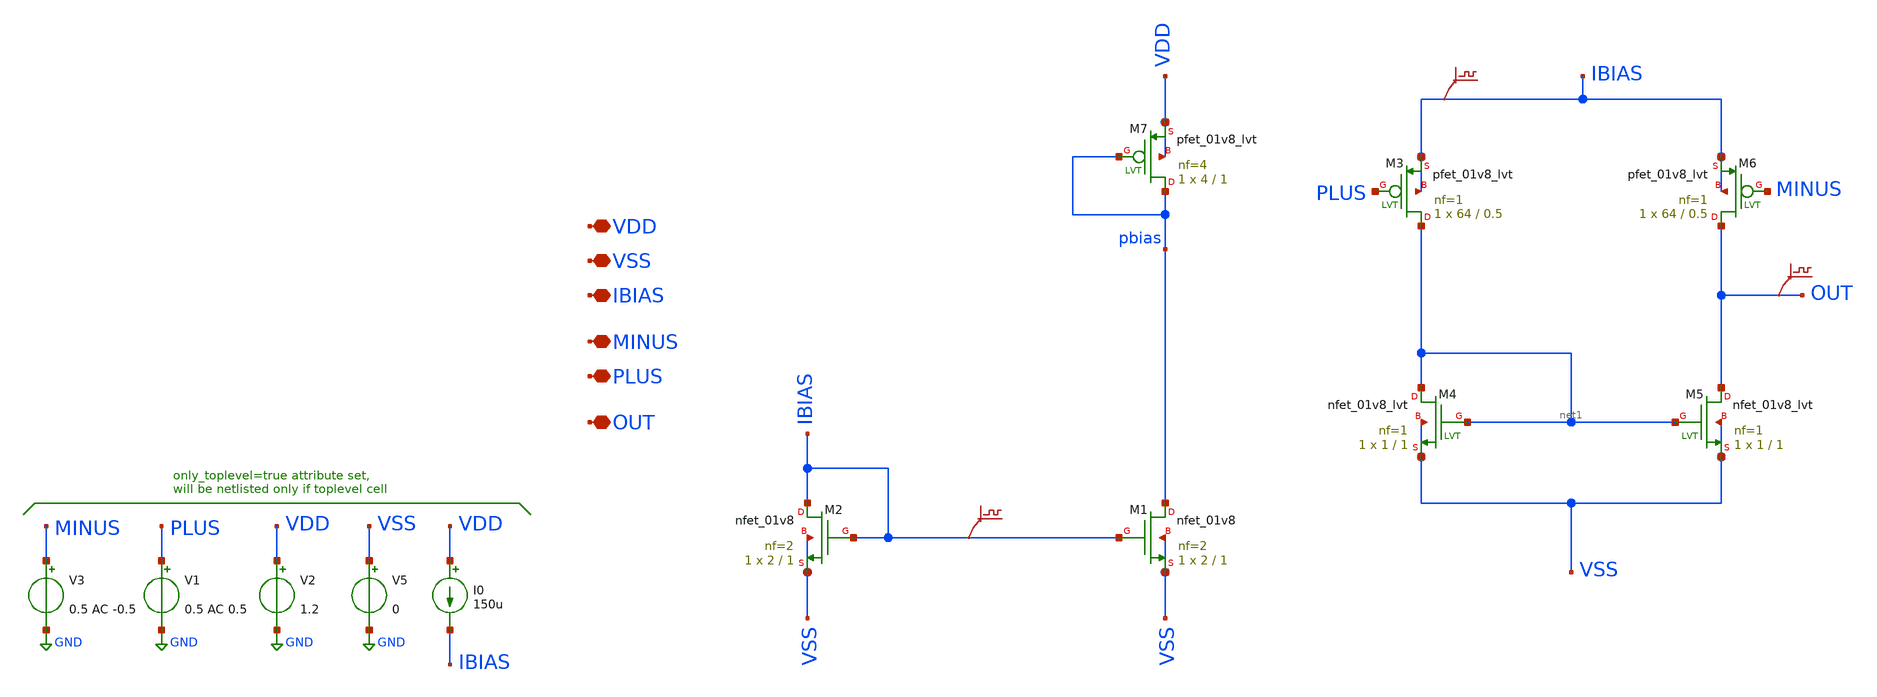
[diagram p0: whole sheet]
** sch_path: q2_opamp.sch
**.subckt q2_opamp VDD VSS MINUS PLUS OUT IBIAS
*.iopin VDD
*.iopin VSS
*.iopin MINUS
*.iopin PLUS
*.iopin OUT
*.iopin IBIAS
V1 PLUS GND 0.5 AC 0.5
V3 MINUS GND 0.5 AC -0.5
V5 VSS GND 0
I0 VDD IBIAS 150u
XM2 IBIAS IBIAS VSS VSS sky130_fd_pr__nfet_01v8 L=1 W=2 nf=2 ad='int((nf+1)/2) * W/nf * 0.29' as='int((nf+2)/2) * W/nf * 0.29'
+ pd='2*int((nf+1)/2) * (W/nf + 0.29)' ps='2*int((nf+2)/2) * (W/nf + 0.29)' nrd='0.29 / W' nrs='0.29 / W'
+ sa=0 sb=0 sd=0 mult=1 m=1
XM1 pbias IBIAS VSS VSS sky130_fd_pr__nfet_01v8 L=1 W=2 nf=2 ad='int((nf+1)/2) * W/nf * 0.29' as='int((nf+2)/2) * W/nf * 0.29'
+ pd='2*int((nf+1)/2) * (W/nf + 0.29)' ps='2*int((nf+2)/2) * (W/nf + 0.29)' nrd='0.29 / W' nrs='0.29 / W'
+ sa=0 sb=0 sd=0 mult=1 m=1
.save v(ibias)
V2 VDD GND 1.2
.save v(out)
XM4 net1 net1 VSS VSS sky130_fd_pr__nfet_01v8_lvt L=1 W=1 nf=1 ad='int((nf+1)/2) * W/nf * 0.29' as='int((nf+2)/2) * W/nf * 0.29'
+ pd='2*int((nf+1)/2) * (W/nf + 0.29)' ps='2*int((nf+2)/2) * (W/nf + 0.29)' nrd='0.29 / W' nrs='0.29 / W'
+ sa=0 sb=0 sd=0 mult=1 m=1
XM5 OUT net1 VSS VSS sky130_fd_pr__nfet_01v8_lvt L=1 W=1 nf=1 ad='int((nf+1)/2) * W/nf * 0.29' as='int((nf+2)/2) * W/nf * 0.29'
+ pd='2*int((nf+1)/2) * (W/nf + 0.29)' ps='2*int((nf+2)/2) * (W/nf + 0.29)' nrd='0.29 / W' nrs='0.29 / W'
+ sa=0 sb=0 sd=0 mult=1 m=1
XM3 net1 PLUS IBIAS IBIAS sky130_fd_pr__pfet_01v8_lvt L=0.5 W=64 nf=1 ad='int((nf+1)/2) * W/nf * 0.29'
+ as='int((nf+2)/2) * W/nf * 0.29' pd='2*int((nf+1)/2) * (W/nf + 0.29)' ps='2*int((nf+2)/2) * (W/nf + 0.29)'
+ nrd='0.29 / W' nrs='0.29 / W' sa=0 sb=0 sd=0 mult=1 m=1
XM6 OUT MINUS IBIAS IBIAS sky130_fd_pr__pfet_01v8_lvt L=0.5 W=64 nf=1 ad='int((nf+1)/2) * W/nf * 0.29'
+ as='int((nf+2)/2) * W/nf * 0.29' pd='2*int((nf+1)/2) * (W/nf + 0.29)' ps='2*int((nf+2)/2) * (W/nf + 0.29)'
+ nrd='0.29 / W' nrs='0.29 / W' sa=0 sb=0 sd=0 mult=1 m=1
XM7 pbias pbias VDD VDD sky130_fd_pr__pfet_01v8_lvt L=1 W=4 nf=4 ad='int((nf+1)/2) * W/nf * 0.29' as='int((nf+2)/2) * W/nf * 0.29'
+ pd='2*int((nf+1)/2) * (W/nf + 0.29)' ps='2*int((nf+2)/2) * (W/nf + 0.29)' nrd='0.29 / W' nrs='0.29 / W'
+ sa=0 sb=0 sd=0 mult=1 m=1
.save v(ibias)
**** begin user architecture code

** opencircuitdesign pdks install
.lib $::SKYWATER_MODELS/sky130.lib.spice tt




.param nw = 1
.param nl = 1
.param pl = 1

.control
let i = 1


dowhile i <= 5
.param pw = i

ac dec 20 1 1000g
plot db(v(out)) 180*cph(v(out))/pi


 *reset
 *ac dec 20 1 1000g
 *plot db(v(out)) 180*cph(v(out))/pi

let i = i + 1
reset
end



*ac dec 20 1 100000g
*run
*plot db(v(out)) 180*cph(v(out))/pi
*reset

*save @m.xm1.msky130_fd_pr__nfet_01v8[gm]
*save @m.xm1.msky130_fd_pr__nfet_01v8[vth]
*save @m.xm1.msky130_fd_pr__nfet_01v8[vdsat]
*save @m.xm1.msky130_fd_pr__nfet_01v8[vds]
*save @m.xm1.msky130_fd_pr__nfet_01v8[id]
*save @m.xm1.msky130_fd_pr__nfet_01v8[gds]
*
*save @m.xm2.msky130_fd_pr__nfet_01v8[gm]
*save @m.xm2.msky130_fd_pr__nfet_01v8[vth]
*save @m.xm2.msky130_fd_pr__nfet_01v8[vdsat]
*save @m.xm2.msky130_fd_pr__nfet_01v8[vds]
*save @m.xm2.msky130_fd_pr__nfet_01v8[id]
*save @m.xm2.msky130_fd_pr__nfet_01v8[gds]
*
*save @m.xm5.msky130_fd_pr__nfet_01v8_lvt[gm]
*save @m.xm5.msky130_fd_pr__nfet_01v8_lvt[vth]
*save @m.xm5.msky130_fd_pr__nfet_01v8_lvt[vdsat]
*save @m.xm5.msky130_fd_pr__nfet_01v8_lvt[vds]
*save @m.xm5.msky130_fd_pr__nfet_01v8_lvt[id]
*save @m.xm5.msky130_fd_pr__nfet_01v8_lvt[gds]
*
*save @m.xm6.msky130_fd_pr__pfet_01v8_lvt[gm]
*save @m.xm6.msky130_fd_pr__pfet_01v8_lvt[vth]
*save @m.xm6.msky130_fd_pr__pfet_01v8_lvt[vdsat]
*save @m.xm6.msky130_fd_pr__pfet_01v8_lvt[vds]
*save @m.xm6.msky130_fd_pr__pfet_01v8_lvt[id]
*save @m.xm6.msky130_fd_pr__pfet_01v8_lvt[gds]


*save all

*op

*write q2_opamp.raw

.endc


**** end user architecture code
**.ends
.GLOBAL GND
.end
